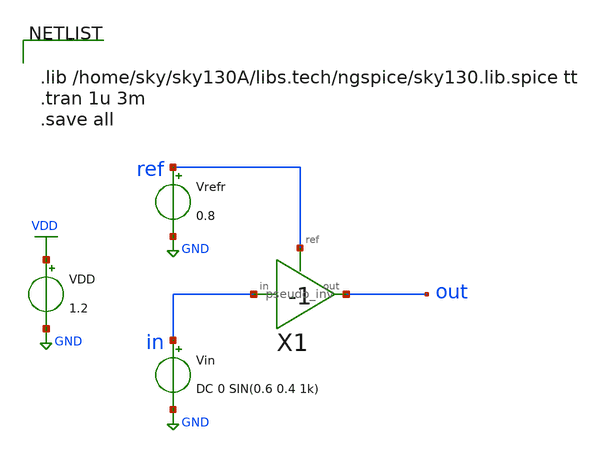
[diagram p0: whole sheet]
** sch_path: xschem/inv/pseudo_inv_tb.sch
**.subckt pseudo_inv_tb
Vin in GND DC 0 SIN(0.6 0.4 1k)
VDD VDD GND 1.2
X1 in out ref pseudo_inv
Vrefr ref GND 0.8
**** begin user architecture code


.lib /home/sky/sky130A/libs.tech/ngspice/sky130.lib.spice tt
.tran 1u 3m
.save all


**** end user architecture code
**.ends
.GLOBAL VDD
.GLOBAL GND
.end
